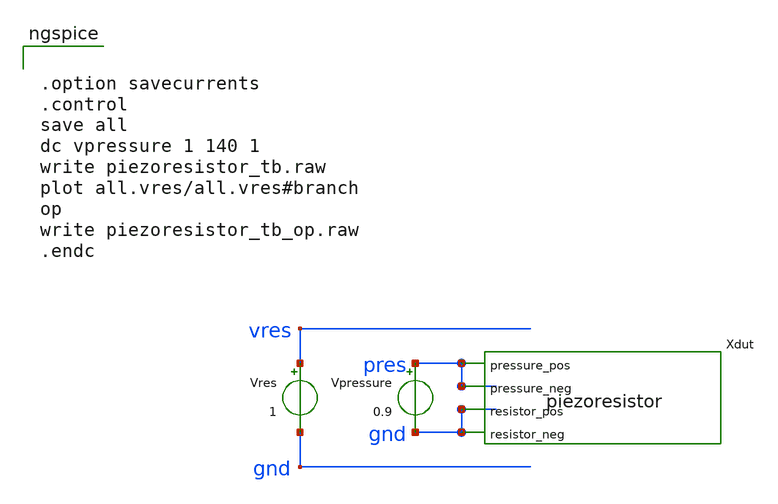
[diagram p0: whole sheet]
** sch_path: piezoresistor_tb.sch
* Copyright 2020 Stefan Frederik Schippers
* Licensed under the Apache License, Version 2.0 (the "License");
* you may not use this file except in compliance with the License.
* You may obtain a copy of the License at
* https://www.apache.org/licenses/LICENSE-2.0
* Unless required by applicable law or agreed to in writing, software
* distributed under the License is distributed on an "AS IS" BASIS,
* WITHOUT WARRANTIES OR CONDITIONS OF ANY KIND, either express or implied.
* See the License for the specific language governing permissions and
* limitations under the License.
**.subckt piezoresistor_tb
Xdut pres pres gnd gnd piezoresistor
Vres vres gnd 1
Vpressure pres gnd 0.9
**** begin user architecture code


.option savecurrents
.control
save all
dc vpressure 1 140 1
write piezoresistor_tb.raw
plot all.vres/all.vres#branch
op
write piezoresistor_tb_op.raw
.endc


**** end user architecture code
**.ends

* expanding   symbol:  piezoresistor.sym # of pins=4
** sym_path: piezoresistor.sym
** sch_path: piezoresistor.sch
.subckt piezoresistor pressure_pos pressure_neg resistor_pos resistor_neg
*.ipin pressure_pos
*.ipin pressure_neg
*.iopin resistor_pos
*.iopin resistor_neg
Broot sqrtp 0 V = sqrt(v(pressure_pos,pressure_neg))
Bres res 0 V = 106*(50/v(sqrtp)-1)*exp(-0.328*v(sqrtp))+15
Brvar resistor_pos resistor_neg I = V(resistor_pos,resistor_neg)/V(res)
.ends

.end
